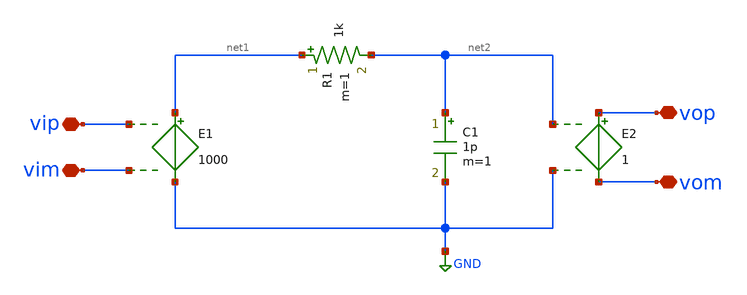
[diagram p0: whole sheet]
** sch_path: xschem/xschem/opa_mod2.sch
**.subckt opa_mod2 vip vim vom vop
*.iopin vip
*.iopin vim
*.iopin vom
*.iopin vop
E1 net1 GND vip vim 1000
E2 vop vom net2 GND 1
R1 net1 net2 1k m=1
C1 net2 GND 1p m=1
**.ends
.GLOBAL GND
.end
